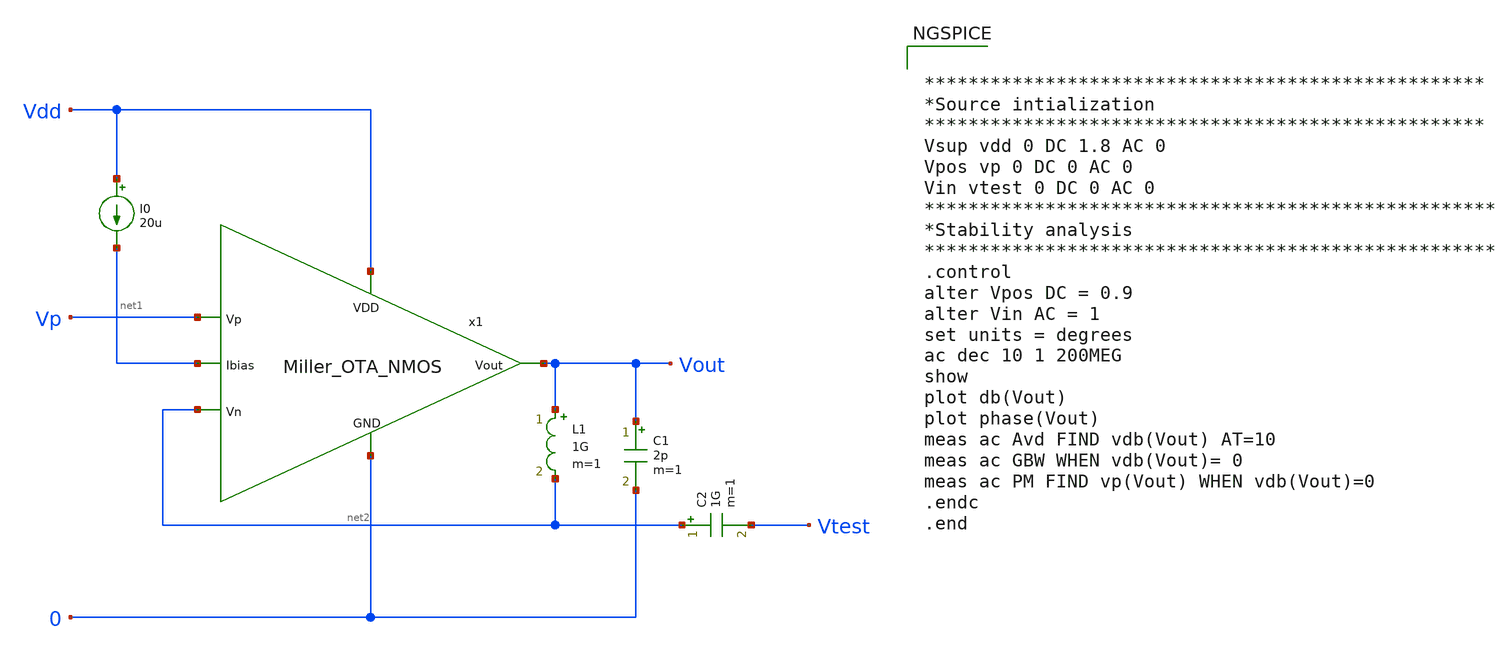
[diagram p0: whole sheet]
** sch_path: Analog_Blocks/OTA/Testbench/Miller_OTA/Transistor5v/Miller_OTA5v_meas_stability.sch
**.subckt Miller_OTA5v_meas_stability
I0 Vdd net1 20u
x1 Vdd net2 Vp Vout net1 0 Miller_OTA_NMOS
L1 Vout net2 1G m=1
C2 net2 Vtest 1G m=1
C1 Vout 0 2p m=1
**** begin user architecture code

.include ~/Analog_blocks/models/skywater-pdk/libraries/sky130_fd_pr/latest/cells/nfet_01v8/sky130_fd_pr__nfet_01v8__tt.corner.spice
.include ~/Analog_blocks/models/skywater-pdk/libraries/sky130_fd_pr/latest/cells/nfet_01v8_lvt/sky130_fd_pr__nfet_01v8_lvt__tt.corner.spice
.include ~/Analog_blocks/models/skywater-pdk/libraries/sky130_fd_pr/latest/cells/pfet_01v8/sky130_fd_pr__pfet_01v8__tt.corner.spice
.include ~/Analog_blocks/models/skywater-pdk/libraries/sky130_fd_pr/latest/cells/nfet_03v3_nvt/sky130_fd_pr__nfet_03v3_nvt__tt.corner.spice
.include ~/Analog_blocks/models/skywater-pdk/libraries/sky130_fd_pr/latest/cells/nfet_05v0_nvt/sky130_fd_pr__nfet_05v0_nvt__tt.corner.spice
.include ~/Analog_blocks/models/skywater-pdk/libraries/sky130_fd_pr/latest/cells/esd_nfet_01v8/sky130_fd_pr__esd_nfet_01v8__tt.corner.spice
.include ~/Analog_blocks/models/skywater-pdk/libraries/sky130_fd_pr/latest/cells/pfet_01v8_lvt/sky130_fd_pr__pfet_01v8_lvt__tt.corner.spice
.include ~/Analog_blocks/models/skywater-pdk/libraries/sky130_fd_pr/latest/cells/pfet_01v8_hvt/sky130_fd_pr__pfet_01v8_hvt__tt.corner.spice
.include ~/Analog_blocks/models/skywater-pdk/libraries/sky130_fd_pr/latest/cells/esd_pfet_g5v0d10v5/sky130_fd_pr__esd_pfet_g5v0d10v5__tt.corner.spice
.include ~/Analog_blocks/models/skywater-pdk/libraries/sky130_fd_pr/latest/cells/pfet_g5v0d10v5/sky130_fd_pr__pfet_g5v0d10v5__tt.corner.spice
.include ~/Analog_blocks/models/skywater-pdk/libraries/sky130_fd_pr/latest/cells/pfet_g5v0d16v0/sky130_fd_pr__pfet_g5v0d16v0__tt.corner.spice
.include ~/Analog_blocks/models/skywater-pdk/libraries/sky130_fd_pr/latest/cells/nfet_g5v0d10v5/sky130_fd_pr__nfet_g5v0d10v5__tt.corner.spice
.include ~/Analog_blocks/models/skywater-pdk/libraries/sky130_fd_pr/latest/cells/nfet_g5v0d16v0/sky130_fd_pr__nfet_g5v0d16v0__tt_discrete.corner.spice
.include ~/Analog_blocks/models/skywater-pdk/libraries/sky130_fd_pr/latest/cells/esd_nfet_g5v0d10v5/sky130_fd_pr__esd_nfet_g5v0d10v5__tt.corner.spice
.include ~/Analog_blocks/models/skywater-pdk/libraries/sky130_fd_pr/latest/models/corners/tt/nonfet.spice
* Mismatch parameters
.include ~/Analog_blocks/models/skywater-pdk/libraries/sky130_fd_pr/latest/cells/nfet_01v8/sky130_fd_pr__nfet_01v8__mismatch.corner.spice
.include ~/Analog_blocks/models/skywater-pdk/libraries/sky130_fd_pr/latest/cells/pfet_01v8/sky130_fd_pr__pfet_01v8__mismatch.corner.spice
.include ~/Analog_blocks/models/skywater-pdk/libraries/sky130_fd_pr/latest/cells/nfet_01v8_lvt/sky130_fd_pr__nfet_01v8_lvt__mismatch.corner.spice
.include ~/Analog_blocks/models/skywater-pdk/libraries/sky130_fd_pr/latest/cells/pfet_01v8_lvt/sky130_fd_pr__pfet_01v8_lvt__mismatch.corner.spice
.include ~/Analog_blocks/models/skywater-pdk/libraries/sky130_fd_pr/latest/cells/pfet_01v8_hvt/sky130_fd_pr__pfet_01v8_hvt__mismatch.corner.spice
.include ~/Analog_blocks/models/skywater-pdk/libraries/sky130_fd_pr/latest/cells/nfet_g5v0d10v5/sky130_fd_pr__nfet_g5v0d10v5__mismatch.corner.spice
.include ~/Analog_blocks/models/skywater-pdk/libraries/sky130_fd_pr/latest/cells/pfet_g5v0d10v5/sky130_fd_pr__pfet_g5v0d10v5__mismatch.corner.spice
.include ~/Analog_blocks/models/skywater-pdk/libraries/sky130_fd_pr/latest/cells/nfet_05v0_nvt/sky130_fd_pr__nfet_05v0_nvt__mismatch.corner.spice
.include ~/Analog_blocks/models/skywater-pdk/libraries/sky130_fd_pr/latest/cells/nfet_03v3_nvt/sky130_fd_pr__nfet_03v3_nvt__mismatch.corner.spice
* Resistor
.include ~/Analog_blocks/models/skywater-pdk/libraries/sky130_fd_pr/latest/models/r+c/res_typical__cap_typical.spice
.include ~/Analog_blocks/models/skywater-pdk/libraries/sky130_fd_pr/latest/models/r+c/res_typical__cap_typical__lin.spice
* Special cells
.include ~/Analog_blocks/models/skywater-pdk/libraries/sky130_fd_pr/latest/models/corners/tt/specialized_cells.spice
* All models
.include ~/Analog_blocks/models/skywater-pdk/libraries/sky130_fd_pr/latest/models/all.spice
* Corner
.include ~/Analog_blocks/models/skywater-pdk/libraries/sky130_fd_pr/latest/models/corners/tt/rf.spice



***************************************************
*Source intialization
***************************************************
Vsup vdd 0 DC 1.8 AC 0
Vpos vp 0 DC 0 AC 0
Vin vtest 0 DC 0 AC 0
****************************************************
*Stability analysis
****************************************************
.control
alter Vpos DC = 0.9
alter Vin AC = 1
set units = degrees
ac dec 10 1 200MEG
show
plot db(Vout)
plot phase(Vout)
meas ac Avd FIND vdb(Vout) AT=10
meas ac GBW WHEN vdb(Vout)= 0
meas ac PM FIND vp(Vout) WHEN vdb(Vout)=0
.endc
.end


**** end user architecture code
**.ends

* expanding   symbol:
*+  /home/eslam/Analog_blocks/Analog_Blocks/OTA/Schematic/Miller_OTA/Transistor5v/Miller_OTA_NMOS.sym # of pins=6
** sym_path: Analog_Blocks/OTA/Schematic/Miller_OTA/Transistor5v/Miller_OTA_NMOS.sym
** sch_path: Analog_Blocks/OTA/Schematic/Miller_OTA/Transistor5v/Miller_OTA_NMOS.sch
.subckt Miller_OTA_NMOS VDD Vn Vp Vout Ibias GND
*.ipin VDD
*.ipin Ibias
*.ipin Vn
*.ipin Vp
*.opin Vout
*.ipin GND
XM1 net1 Vn net3 GND sky130_fd_pr__nfet_g5v0d10v5 L=0.5 W=10 nf=1 ad='int((nf+1)/2) * W/nf * 0.29' as='int((nf+2)/2) * W/nf * 0.29'
+ pd='2*int((nf+1)/2) * (W/nf + 0.29)' ps='2*int((nf+2)/2) * (W/nf + 0.29)' nrd='0.29 / W' nrs='0.29 / W'
+ sa=0 sb=0 sd=0 mult=8 m=8
XM2 net2 Vp net3 GND sky130_fd_pr__nfet_g5v0d10v5 L=0.5 W=10 nf=1 ad='int((nf+1)/2) * W/nf * 0.29' as='int((nf+2)/2) * W/nf * 0.29'
+ pd='2*int((nf+1)/2) * (W/nf + 0.29)' ps='2*int((nf+2)/2) * (W/nf + 0.29)' nrd='0.29 / W' nrs='0.29 / W'
+ sa=0 sb=0 sd=0 mult=8 m=8
XM3 net1 net1 VDD VDD sky130_fd_pr__pfet_g5v0d10v5 L=0.5 W=5 nf=1 ad='int((nf+1)/2) * W/nf * 0.29' as='int((nf+2)/2) * W/nf * 0.29'
+ pd='2*int((nf+1)/2) * (W/nf + 0.29)' ps='2*int((nf+2)/2) * (W/nf + 0.29)' nrd='0.29 / W' nrs='0.29 / W'
+ sa=0 sb=0 sd=0 mult=4 m=4
XM4 net2 net1 VDD VDD sky130_fd_pr__pfet_g5v0d10v5 L=0.5 W=5 nf=1 ad='int((nf+1)/2) * W/nf * 0.29' as='int((nf+2)/2) * W/nf * 0.29'
+ pd='2*int((nf+1)/2) * (W/nf + 0.29)' ps='2*int((nf+2)/2) * (W/nf + 0.29)' nrd='0.29 / W' nrs='0.29 / W'
+ sa=0 sb=0 sd=0 mult=4 m=4
XM6 Vout net2 VDD VDD sky130_fd_pr__pfet_g5v0d10v5 L=0.5 W=5 nf=1 ad='int((nf+1)/2) * W/nf * 0.29' as='int((nf+2)/2) * W/nf * 0.29'
+ pd='2*int((nf+1)/2) * (W/nf + 0.29)' ps='2*int((nf+2)/2) * (W/nf + 0.29)' nrd='0.29 / W' nrs='0.29 / W'
+ sa=0 sb=0 sd=0 mult=20 m=20
XM5 net3 Ibias GND GND sky130_fd_pr__nfet_g5v0d10v5 L=1 W=3 nf=1 ad='int((nf+1)/2) * W/nf * 0.29' as='int((nf+2)/2) * W/nf * 0.29'
+ pd='2*int((nf+1)/2) * (W/nf + 0.29)' ps='2*int((nf+2)/2) * (W/nf + 0.29)' nrd='0.29 / W' nrs='0.29 / W'
+ sa=0 sb=0 sd=0 mult=8 m=8
XM8 Ibias Ibias GND GND sky130_fd_pr__nfet_g5v0d10v5 L=1 W=3 nf=1 ad='int((nf+1)/2) * W/nf * 0.29' as='int((nf+2)/2) * W/nf * 0.29'
+ pd='2*int((nf+1)/2) * (W/nf + 0.29)' ps='2*int((nf+2)/2) * (W/nf + 0.29)' nrd='0.29 / W' nrs='0.29 / W'
+ sa=0 sb=0 sd=0 mult=8 m=8
XC1 net2 Vout sky130_fd_pr__cap_mim_m3_2 W=27.3 L=27.3 MF=2 m=2
XM7 Vout Ibias GND GND sky130_fd_pr__nfet_g5v0d10v5 L=1 W=3 nf=1 ad='int((nf+1)/2) * W/nf * 0.29' as='int((nf+2)/2) * W/nf * 0.29'
+ pd='2*int((nf+1)/2) * (W/nf + 0.29)' ps='2*int((nf+2)/2) * (W/nf + 0.29)' nrd='0.29 / W' nrs='0.29 / W'
+ sa=0 sb=0 sd=0 mult=16 m=16
.ends

.end
